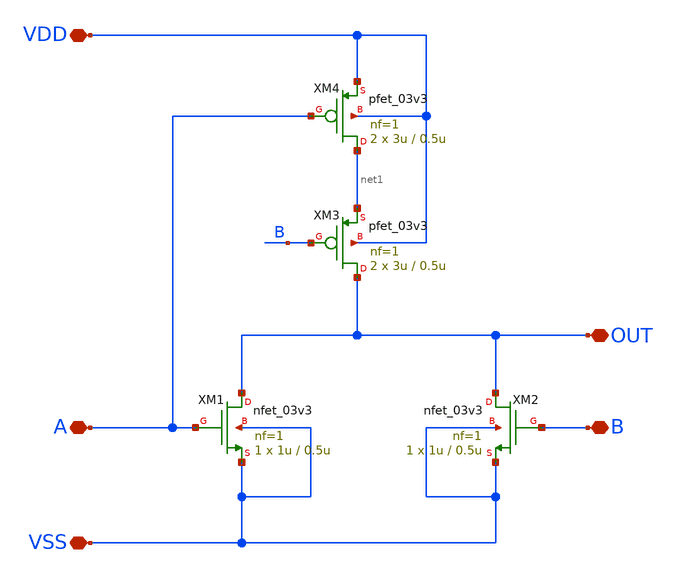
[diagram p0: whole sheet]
** sch_path: designs/FinalBlocksLayout/nor2/nor2.sch
**.subckt nor2 VDD VSS B A OUT
*.iopin VDD
*.iopin VSS
*.iopin B
*.iopin A
*.iopin OUT
XM1 OUT A VSS VSS nfet_03v3 L=0.5u W=1u nf=1 ad='int((nf+1)/2) * W/nf * 0.18u' as='int((nf+2)/2) * W/nf * 0.18u'
+ pd='2*int((nf+1)/2) * (W/nf + 0.18u)' ps='2*int((nf+2)/2) * (W/nf + 0.18u)' nrd='0.18u / W' nrs='0.18u / W'
+ sa=0 sb=0 sd=0 m=1
XM2 OUT B VSS VSS nfet_03v3 L=0.5u W=1u nf=1 ad='int((nf+1)/2) * W/nf * 0.18u' as='int((nf+2)/2) * W/nf * 0.18u'
+ pd='2*int((nf+1)/2) * (W/nf + 0.18u)' ps='2*int((nf+2)/2) * (W/nf + 0.18u)' nrd='0.18u / W' nrs='0.18u / W'
+ sa=0 sb=0 sd=0 m=1
XM3 OUT B net1 VDD pfet_03v3 L=0.5u W=3u nf=1 ad='int((nf+1)/2) * W/nf * 0.18u' as='int((nf+2)/2) * W/nf * 0.18u'
+ pd='2*int((nf+1)/2) * (W/nf + 0.18u)' ps='2*int((nf+2)/2) * (W/nf + 0.18u)' nrd='0.18u / W' nrs='0.18u / W'
+ sa=0 sb=0 sd=0 m=2
XM4 net1 A VDD VDD pfet_03v3 L=0.5u W=3u nf=1 ad='int((nf+1)/2) * W/nf * 0.18u' as='int((nf+2)/2) * W/nf * 0.18u'
+ pd='2*int((nf+1)/2) * (W/nf + 0.18u)' ps='2*int((nf+2)/2) * (W/nf + 0.18u)' nrd='0.18u / W' nrs='0.18u / W'
+ sa=0 sb=0 sd=0 m=2
**.ends
.end
